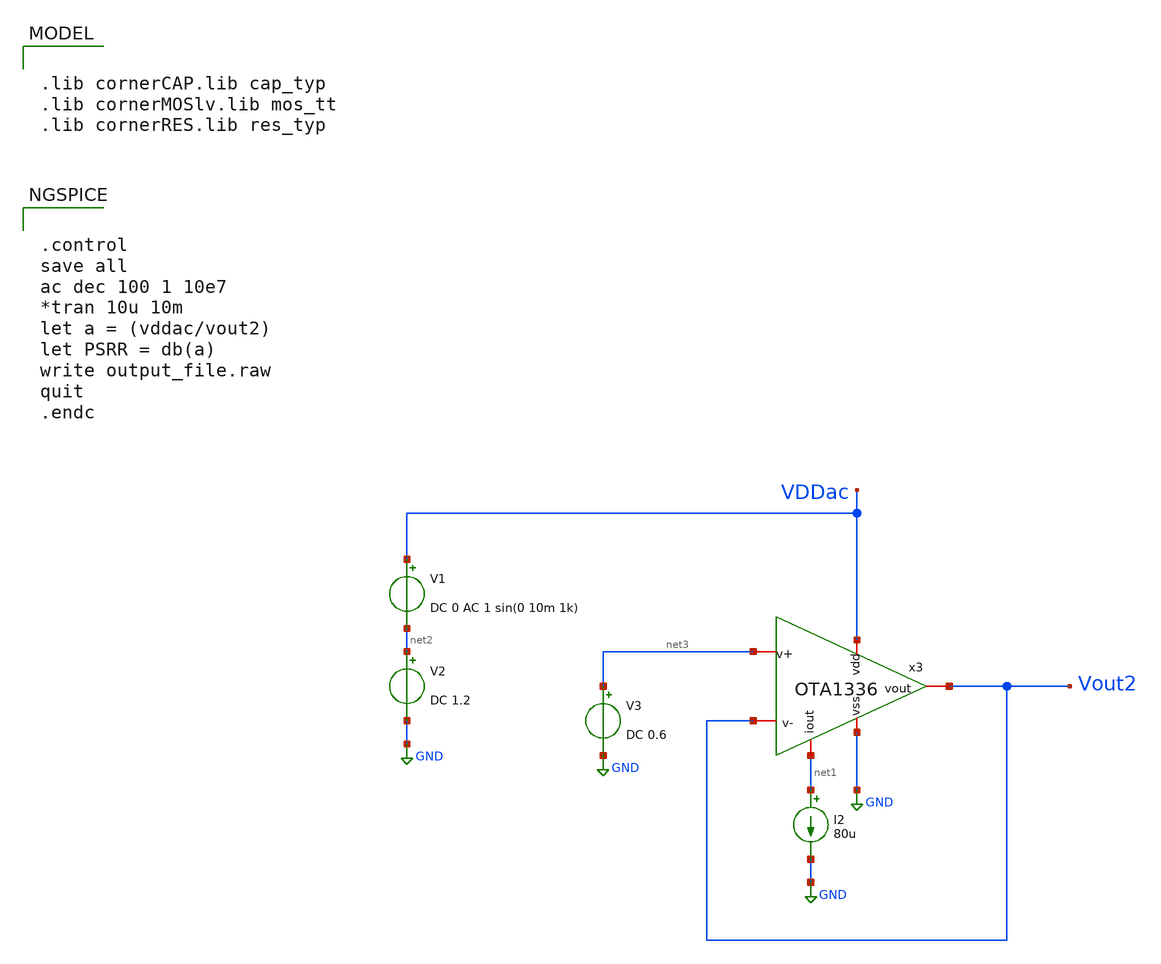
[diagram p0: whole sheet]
** sch_path: tests/data/OTA1336/testbenches/ac/xschem/OTA1336_psrr_tb.sch
**.subckt OTA1336_psrr_tb
I2 net1 GND 80u
V2 net2 GND DC 1.2
x3 VDDac net1 Vout2 Vout2 net3 GND OTA1336
V1 VDDac net2 DC 0 AC 1 sin(0 10m 1k)
V3 net3 GND DC 0.6
**** begin user architecture code

.lib cornerCAP.lib cap_typ
.lib cornerMOSlv.lib mos_tt
.lib cornerRES.lib res_typ



.control
save all
ac dec 100 1 10e7
*tran 10u 10m
let a = (vddac/vout2)
let PSRR = db(a)
write output_file.raw
quit
.endc


**** end user architecture code
**.ends
.GLOBAL GND
.end
